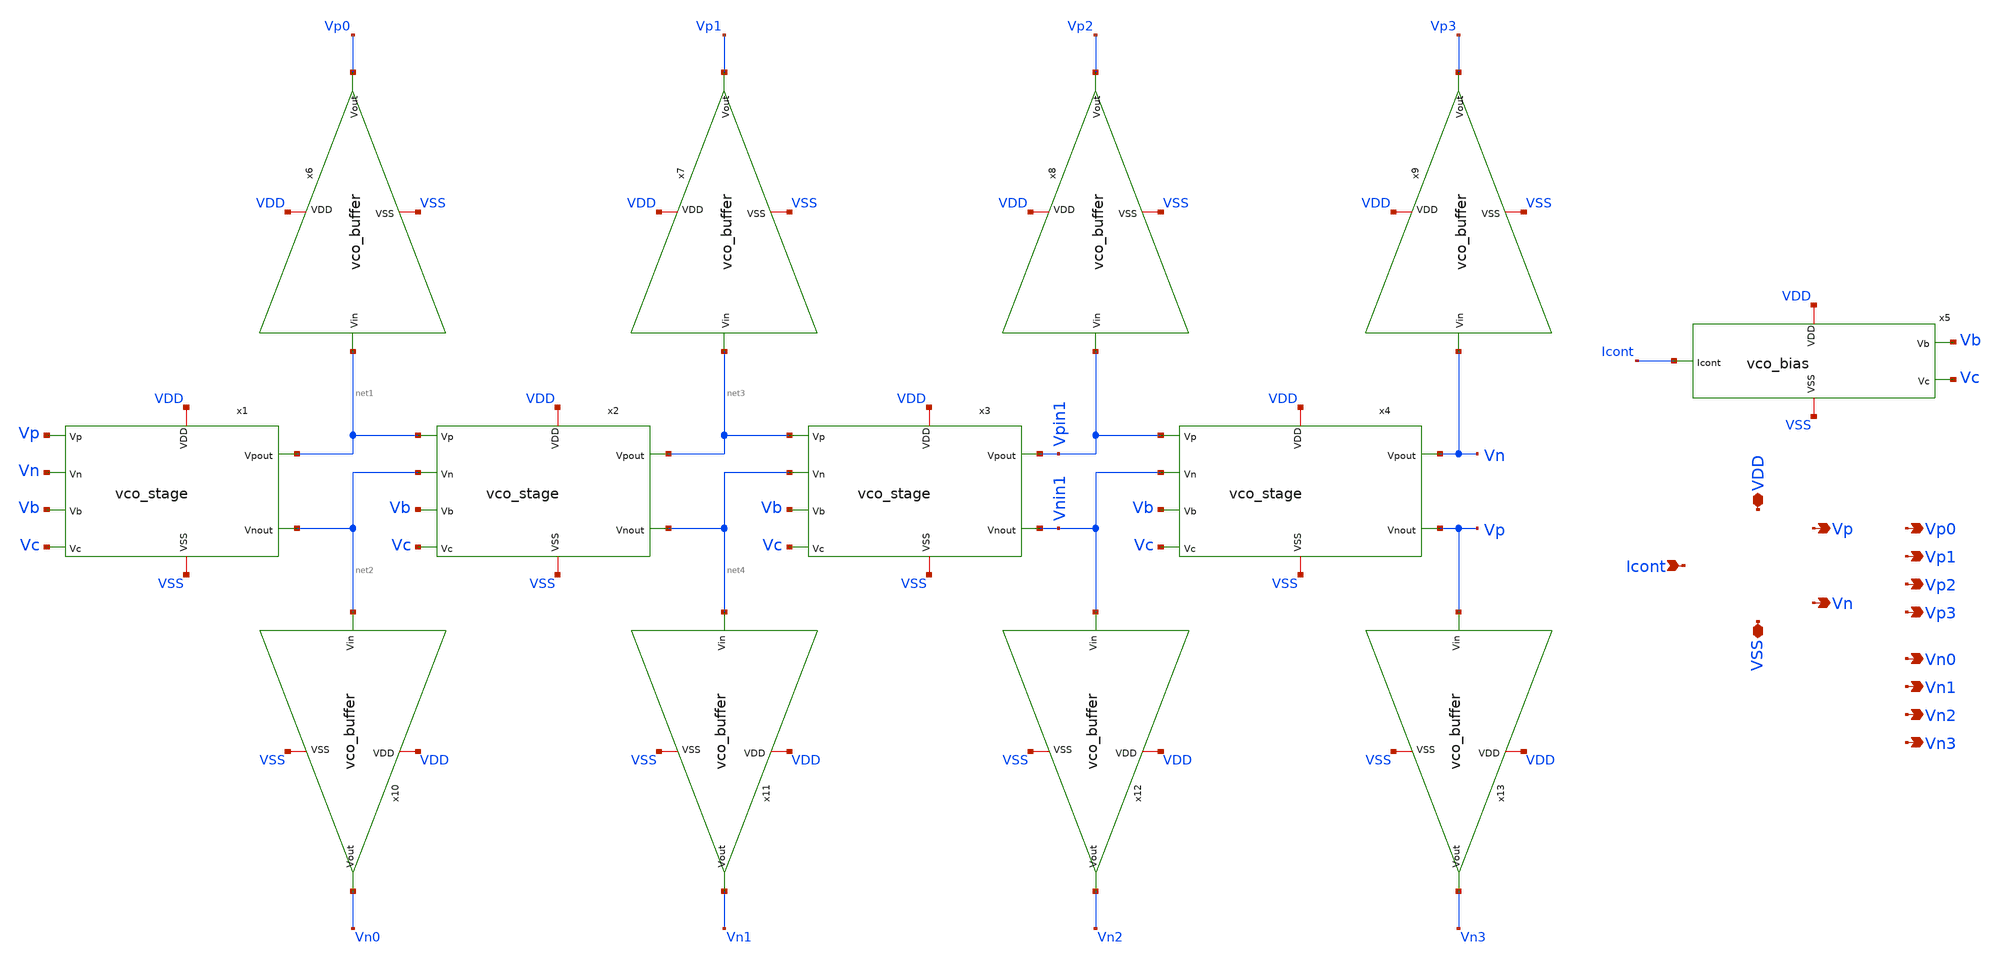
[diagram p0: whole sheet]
** sch_path: xschem/vco.sch
**.subckt vco VDD VSS Icont Vp Vn Vp0 Vp1 Vp2 Vp3 Vn0 Vn1 Vn2 Vn3
*.iopin VDD
*.iopin VSS
*.ipin Icont
*.opin Vp
*.opin Vn
*.opin Vp0
*.opin Vp1
*.opin Vp2
*.opin Vp3
*.opin Vn0
*.opin Vn1
*.opin Vn2
*.opin Vn3
x1 VDD VSS Vp Vn Vb Vc net1 net2 vco_stage
x2 VDD VSS net1 net2 Vb Vc net3 net4 vco_stage
x3 VDD VSS net3 net4 Vb Vc Vpin1 Vnin1 vco_stage
x4 VDD VSS Vpin1 Vnin1 Vb Vc Vn Vp vco_stage
x5 VDD VSS Icont Vb Vc vco_bias
x6 VDD VSS net1 Vp0 vco_buffer
x7 VDD VSS net3 Vp1 vco_buffer
x8 VDD VSS Vpin1 Vp2 vco_buffer
x9 VDD VSS Vn Vp3 vco_buffer
x10 VDD VSS net2 Vn0 vco_buffer
x11 VDD VSS net4 Vn1 vco_buffer
x12 VDD VSS Vnin1 Vn2 vco_buffer
x13 VDD VSS Vp Vn3 vco_buffer
**.ends

* expanding   symbol:  vco_stage.sym # of pins=8
** sym_path: xschem/vco_stage.sym
** sch_path: xschem/vco_stage.sch
.subckt vco_stage VDD VSS Vp Vn Vb Vc Vpout Vnout
*.iopin VDD
*.iopin VSS
*.ipin Vp
*.ipin Vn
*.ipin Vb
*.ipin Vc
*.opin Vpout
*.opin Vnout
XM5 Vds_m5 Vc VSS VSS sky130_fd_pr__nfet_01v8 L={L} W={W} nf=2 ad='int((nf+1)/2) * W/nf * 0.29' as='int((nf+2)/2) * W/nf * 0.29'
+ pd='2*int((nf+1)/2) * (W/nf + 0.29)' ps='2*int((nf+2)/2) * (W/nf + 0.29)' nrd='0.29 / W' nrs='0.29 / W'
+ sa=0 sb=0 sd=0 mult=1 m=1
x1 VDD VSS Vp Vb Vnout Vpout Vds_m5 vco_stage_half
x2 VDD VSS Vn Vb Vpout Vnout Vds_m5 vco_stage_half
.ends


* expanding   symbol:  vco_bias.sym # of pins=5
** sym_path: xschem/vco_bias.sym
** sch_path: xschem/vco_bias.sch
.subckt vco_bias VDD VSS Icont Vb Vc
*.iopin VDD
*.iopin VSS
*.ipin Icont
*.opin Vb
*.opin Vc
XM1 Icont Icont VSS VSS sky130_fd_pr__nfet_01v8 L=0.15 W=2 nf=1 ad='int((nf+1)/2) * W/nf * 0.29' as='int((nf+2)/2) * W/nf * 0.29'
+ pd='2*int((nf+1)/2) * (W/nf + 0.29)' ps='2*int((nf+2)/2) * (W/nf + 0.29)' nrd='0.29 / W' nrs='0.29 / W'
+ sa=0 sb=0 sd=0 mult=1 m=1
XM2 Vb Icont VSS VSS sky130_fd_pr__nfet_01v8 L=0.15 W=1 nf=1 ad='int((nf+1)/2) * W/nf * 0.29' as='int((nf+2)/2) * W/nf * 0.29'
+ pd='2*int((nf+1)/2) * (W/nf + 0.29)' ps='2*int((nf+2)/2) * (W/nf + 0.29)' nrd='0.29 / W' nrs='0.29 / W'
+ sa=0 sb=0 sd=0 mult=1 m=1
XM3 VDD Vb Vb VDD sky130_fd_pr__nfet_01v8 L=0.15 W=2 nf=1 ad='int((nf+1)/2) * W/nf * 0.29' as='int((nf+2)/2) * W/nf * 0.29'
+ pd='2*int((nf+1)/2) * (W/nf + 0.29)' ps='2*int((nf+2)/2) * (W/nf + 0.29)' nrd='0.29 / W' nrs='0.29 / W'
+ sa=0 sb=0 sd=0 mult=1 m=1
V1 Vc Icont 0
.ends


* expanding   symbol:  vco_buffer.sym # of pins=4
** sym_path: xschem/vco_buffer.sym
** sch_path: xschem/vco_buffer.sch
.subckt vco_buffer VDD VSS Vin Vout
*.iopin VDD
*.iopin VSS
*.ipin Vin
*.opin Vout
x1 VDD Vin net1 VSS vco_inverter
x2 VDD net1 Vout VSS vco_inverter
.ends


* expanding   symbol:  vco_stage_half.sym # of pins=7
** sym_path: xschem/vco_stage_half.sym
** sch_path: xschem/vco_stage_half.sch
.subckt vco_stage_half VDD VSS Vin Vb Vd Vout Vs
*.iopin VDD
*.iopin VSS
*.ipin Vin
*.ipin Vb
*.ipin Vd
*.opin Vout
*.opin Vs
XM8 VSS Vout VSS VSS sky130_fd_pr__nfet_01v8 L={WLcap} W={WLcap} nf=1 ad='int((nf+1)/2) * W/nf * 0.29'
+ as='int((nf+2)/2) * W/nf * 0.29' pd='2*int((nf+1)/2) * (W/nf + 0.29)' ps='2*int((nf+2)/2) * (W/nf + 0.29)'
+ nrd='0.29 / W' nrs='0.29 / W' sa=0 sb=0 sd=0 mult=1 m=1
XM7 Vout Vd VDD VDD sky130_fd_pr__pfet_01v8 L={L} W={W} nf=2 ad='int((nf+1)/2) * W/nf * 0.29' as='int((nf+2)/2) * W/nf * 0.29'
+ pd='2*int((nf+1)/2) * (W/nf + 0.29)' ps='2*int((nf+2)/2) * (W/nf + 0.29)' nrd='0.29 / W' nrs='0.29 / W'
+ sa=0 sb=0 sd=0 mult=1 m=1
XM3 Vout Vb VDD VDD sky130_fd_pr__pfet_01v8 L={L} W={W} nf=2 ad='int((nf+1)/2) * W/nf * 0.29' as='int((nf+2)/2) * W/nf * 0.29'
+ pd='2*int((nf+1)/2) * (W/nf + 0.29)' ps='2*int((nf+2)/2) * (W/nf + 0.29)' nrd='0.29 / W' nrs='0.29 / W'
+ sa=0 sb=0 sd=0 mult=1 m=1
XM1 Vout Vin Vs VSS sky130_fd_pr__nfet_01v8 L={L} W={W} nf=2 ad='int((nf+1)/2) * W/nf * 0.29' as='int((nf+2)/2) * W/nf * 0.29'
+ pd='2*int((nf+1)/2) * (W/nf + 0.29)' ps='2*int((nf+2)/2) * (W/nf + 0.29)' nrd='0.29 / W' nrs='0.29 / W'
+ sa=0 sb=0 sd=0 mult=1 m=1
.ends


* expanding   symbol:  vco_inverter.sym # of pins=4
** sym_path: xschem/vco_inverter.sym
** sch_path: xschem/vco_inverter.sch
.subckt vco_inverter VDD Vin Vout VSS
*.iopin VDD
*.iopin VSS
*.ipin Vin
*.opin Vout
XM1 Vout Vin VSS VSS sky130_fd_pr__nfet_01v8 L=0.15 W=1 nf=1 ad='int((nf+1)/2) * W/nf * 0.29' as='int((nf+2)/2) * W/nf * 0.29'
+ pd='2*int((nf+1)/2) * (W/nf + 0.29)' ps='2*int((nf+2)/2) * (W/nf + 0.29)' nrd='0.29 / W' nrs='0.29 / W'
+ sa=0 sb=0 sd=0 mult=1 m=1
XM2 Vout Vin VDD VDD sky130_fd_pr__pfet_01v8 L=0.15 W=1 nf=1 ad='int((nf+1)/2) * W/nf * 0.29' as='int((nf+2)/2) * W/nf * 0.29'
+ pd='2*int((nf+1)/2) * (W/nf + 0.29)' ps='2*int((nf+2)/2) * (W/nf + 0.29)' nrd='0.29 / W' nrs='0.29 / W'
+ sa=0 sb=0 sd=0 mult=1 m=1
.ends

.end
